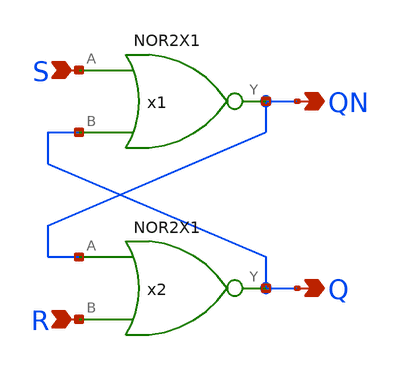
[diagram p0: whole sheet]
** sch_path: layout/xschem/sky130_rhbd/SRLATCH.sch
**.subckt SRLATCH S R QN Q
*.ipin S
*.ipin R
*.opin QN
*.opin Q
x1 QN S Q VDD VSS NOR2X1
x2 Q QN R VDD VSS NOR2X1
**.ends
.end
